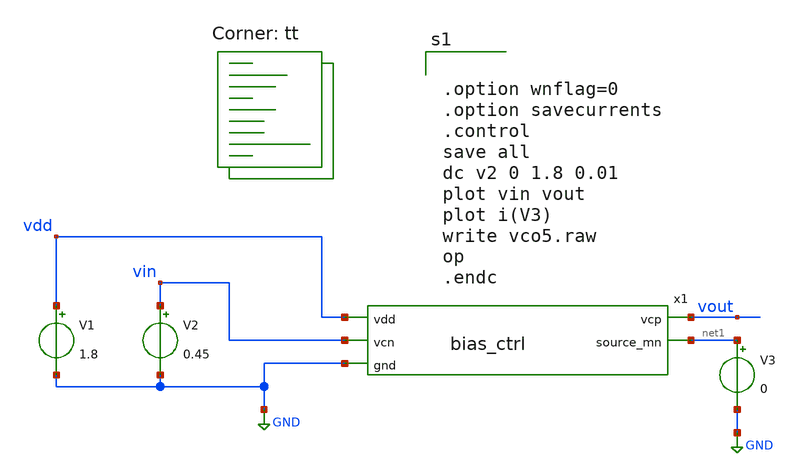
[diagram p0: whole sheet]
** sch_path: xsch/bias_ctrl_tb.sch
**.subckt bias_ctrl_tb
V1 vdd GND 1.8
V2 vin GND 0.45
x1 vdd vout vin net1 GND bias_ctrl
V3 net1 GND 0
**** begin user architecture code
.lib $::SKYWATER_MODELS/sky130.lib.spice tt


.option wnflag=0
.option savecurrents
.control
save all
dc v2 0 1.8 0.01
plot vin vout
plot i(V3)
write vco5.raw
op
.endc


**** end user architecture code
**.ends

* expanding   symbol:  bias_ctrl.sym # of pins=5
** sym_path: xsch/bias_ctrl.sym
** sch_path: xsch/bias_ctrl.sch
.subckt bias_ctrl vdd vcp vcn source_mn gnd
*.ipin vcn
*.ipin vdd
*.ipin gnd
*.opin vcp
*.opin source_mn
XM2 vcp vcp vdd vdd sky130_fd_pr__pfet_01v8 L=0.3 W=4 nf=1 ad='int((nf+1)/2) * W/nf * 0.29' as='int((nf+2)/2) * W/nf * 0.29'
+ pd='2*int((nf+1)/2) * (W/nf + 0.29)' ps='2*int((nf+2)/2) * (W/nf + 0.29)' nrd='0.29 / W' nrs='0.29 / W'
+ sa=0 sb=0 sd=0 mult=1 m=1
XM1 vcp vcn source_mn gnd sky130_fd_pr__nfet_01v8 L=0.3 W=1 nf=1 ad='int((nf+1)/2) * W/nf * 0.29' as='int((nf+2)/2) * W/nf * 0.29'
+ pd='2*int((nf+1)/2) * (W/nf + 0.29)' ps='2*int((nf+2)/2) * (W/nf + 0.29)' nrd='0.29 / W' nrs='0.29 / W'
+ sa=0 sb=0 sd=0 mult=1 m=1
.ends

.GLOBAL GND
.end
